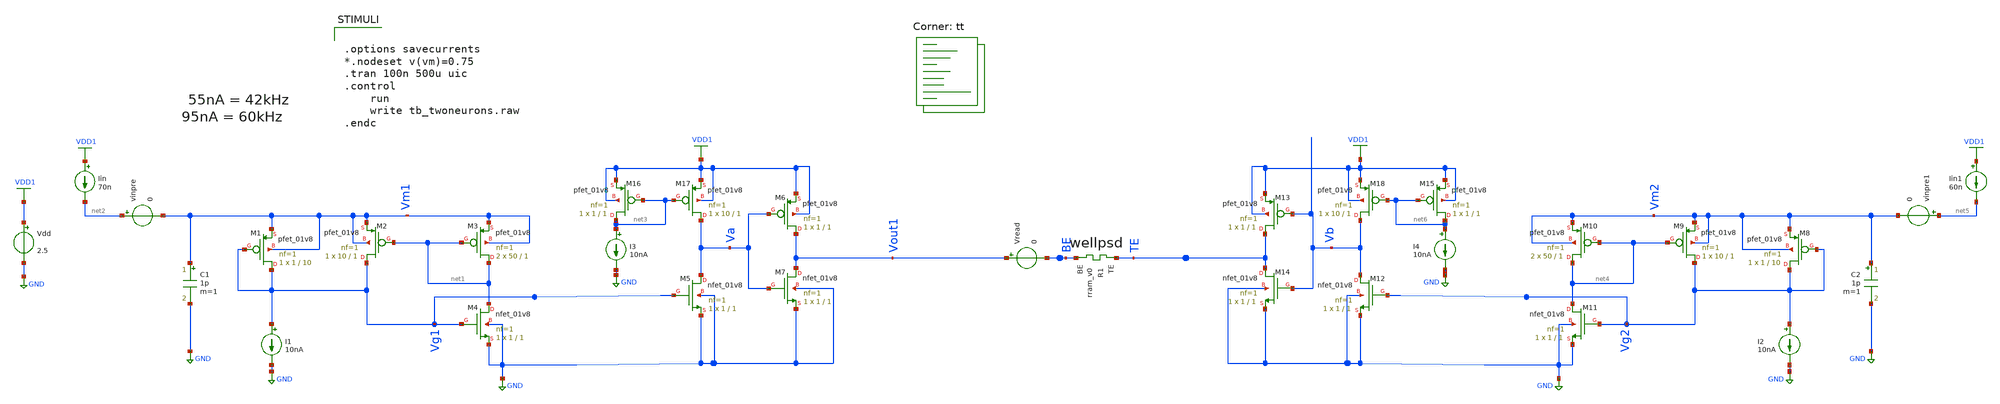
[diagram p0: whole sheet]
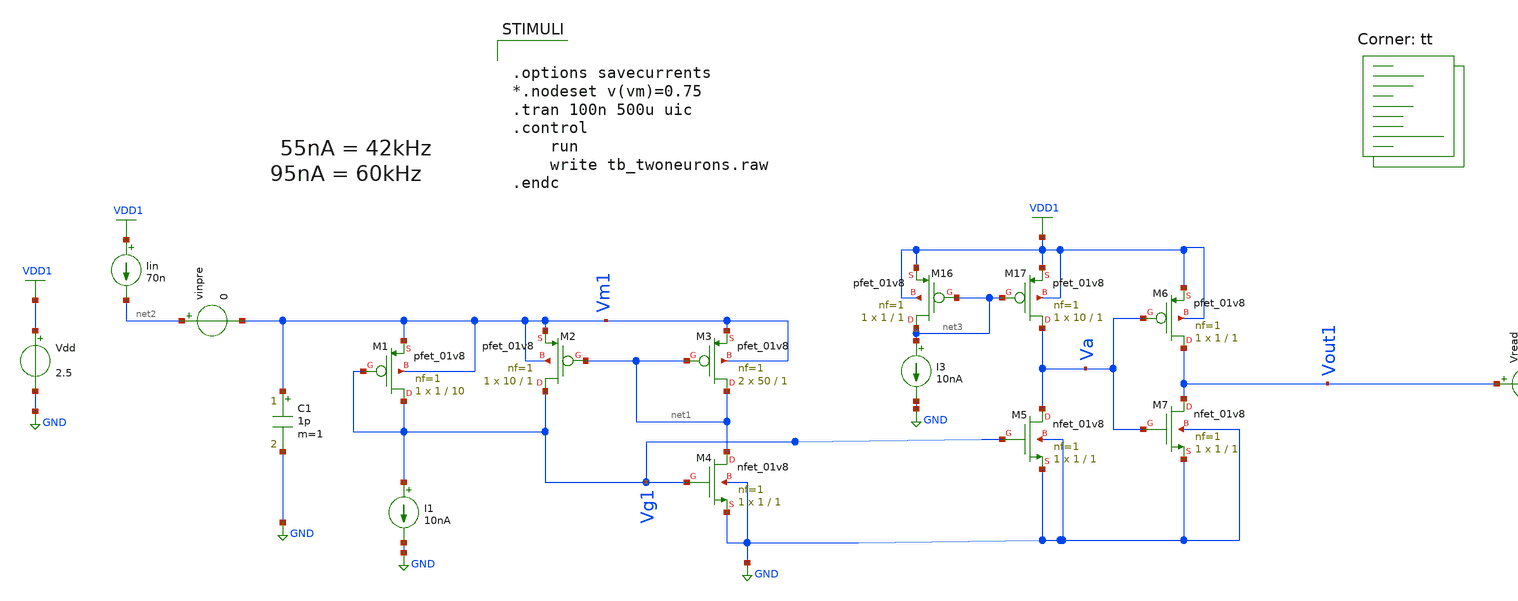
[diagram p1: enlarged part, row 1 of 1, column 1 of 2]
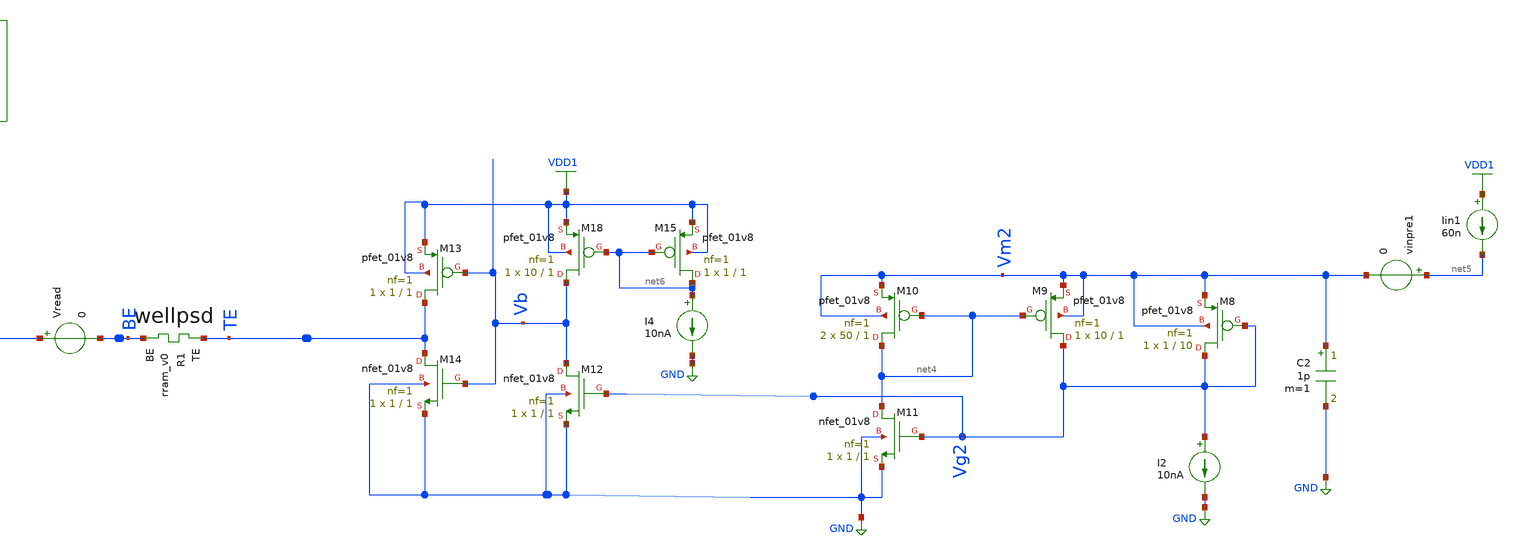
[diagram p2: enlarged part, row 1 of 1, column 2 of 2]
** sch_path: Neuron/ultralif/tb_twoneurons.sch
**.subckt tb_twoneurons
XM1 Vg1 Vg1 Vm1 Vm1 sky130_fd_pr__pfet_01v8 L=10 W=1 nf=1 ad='int((nf+1)/2) * W/nf * 0.29' as='int((nf+2)/2) * W/nf * 0.29'
+ pd='2*int((nf+1)/2) * (W/nf + 0.29)' ps='2*int((nf+2)/2) * (W/nf + 0.29)' nrd='0.29 / W' nrs='0.29 / W'
+ sa=0 sb=0 sd=0 mult=1 m=1
XM2 Vg1 net1 Vm1 Vm1 sky130_fd_pr__pfet_01v8 L=1 W=10 nf=1 ad='int((nf+1)/2) * W/nf * 0.29' as='int((nf+2)/2) * W/nf * 0.29'
+ pd='2*int((nf+1)/2) * (W/nf + 0.29)' ps='2*int((nf+2)/2) * (W/nf + 0.29)' nrd='0.29 / W' nrs='0.29 / W'
+ sa=0 sb=0 sd=0 mult=1 m=1
XM3 net1 net1 Vm1 Vm1 sky130_fd_pr__pfet_01v8 L=1 W=50 nf=1 ad='int((nf+1)/2) * W/nf * 0.29' as='int((nf+2)/2) * W/nf * 0.29'
+ pd='2*int((nf+1)/2) * (W/nf + 0.29)' ps='2*int((nf+2)/2) * (W/nf + 0.29)' nrd='0.29 / W' nrs='0.29 / W'
+ sa=0 sb=0 sd=0 mult=2 m=2
XM4 net1 Vg1 GND GND sky130_fd_pr__nfet_01v8 L=1 W=1 nf=1 ad='int((1 + 1)/2) * 1 / 1 * 0.29' as='int((1 + 2)/2) * 1 / 1 * 0.29'
+ pd='2*int((1 + 1)/2) * (1 / 1 + 0.29)' ps='2*int((1 + 2)/2) * (1 / 1 + 0.29)' nrd='0.29 / 1 ' nrs='0.29 / 1 '
+ sa=0 sb=0 sd=0 mult=1 m=1
XM5 Va Vg1 GND GND sky130_fd_pr__nfet_01v8 L=1 W=1 nf=1 ad='int((1 + 1)/2) * 1 / 1 * 0.29' as='int((1 + 2)/2) * 1 / 1 * 0.29'
+ pd='2*int((1 + 1)/2) * (1 / 1 + 0.29)' ps='2*int((1 + 2)/2) * (1 / 1 + 0.29)' nrd='0.29 / 1 ' nrs='0.29 / 1 '
+ sa=0 sb=0 sd=0 mult=1 m=1
XM6 Vout1 Va VDD1 VDD1 sky130_fd_pr__pfet_01v8 L=1 W=1 nf=1 ad='int((nf+1)/2) * W/nf * 0.29' as='int((nf+2)/2) * W/nf * 0.29'
+ pd='2*int((nf+1)/2) * (W/nf + 0.29)' ps='2*int((nf+2)/2) * (W/nf + 0.29)' nrd='0.29 / W' nrs='0.29 / W'
+ sa=0 sb=0 sd=0 mult=1 m=1
XM7 Vout1 Va GND GND sky130_fd_pr__nfet_01v8 L=1 W=1 nf=1 ad='int((1 + 1)/2) * 1 / 1 * 0.29' as='int((1 + 2)/2) * 1 / 1 * 0.29'
+ pd='2*int((1 + 1)/2) * (1 / 1 + 0.29)' ps='2*int((1 + 2)/2) * (1 / 1 + 0.29)' nrd='0.29 / 1 ' nrs='0.29 / 1 '
+ sa=0 sb=0 sd=0 mult=1 m=1
I1 Vg1 GND 10nA
C1 Vm1 GND 1p m=1
Iin VDD1 net2 70n
I3 net3 GND 10nA
Vdd VDD1 GND 2.5
XR1 TE BE rram_v0
vinpre net2 Vm1 0
XM16 net3 net3 VDD1 VDD1 sky130_fd_pr__pfet_01v8 L=1 W=1 nf=1 ad='int((nf+1)/2) * W/nf * 0.29' as='int((nf+2)/2) * W/nf * 0.29'
+ pd='2*int((nf+1)/2) * (W/nf + 0.29)' ps='2*int((nf+2)/2) * (W/nf + 0.29)' nrd='0.29 / W' nrs='0.29 / W'
+ sa=0 sb=0 sd=0 mult=1 m=1
XM17 Va net3 VDD1 VDD1 sky130_fd_pr__pfet_01v8 L=1 W=10 nf=1 ad='int((nf+1)/2) * W/nf * 0.29' as='int((nf+2)/2) * W/nf * 0.29'
+ pd='2*int((nf+1)/2) * (W/nf + 0.29)' ps='2*int((nf+2)/2) * (W/nf + 0.29)' nrd='0.29 / W' nrs='0.29 / W'
+ sa=0 sb=0 sd=0 mult=1 m=1
XM8 Vg2 Vg2 Vm2 Vm2 sky130_fd_pr__pfet_01v8 L=10 W=1 nf=1 ad='int((nf+1)/2) * W/nf * 0.29' as='int((nf+2)/2) * W/nf * 0.29'
+ pd='2*int((nf+1)/2) * (W/nf + 0.29)' ps='2*int((nf+2)/2) * (W/nf + 0.29)' nrd='0.29 / W' nrs='0.29 / W'
+ sa=0 sb=0 sd=0 mult=1 m=1
XM9 Vg2 net4 Vm2 Vm2 sky130_fd_pr__pfet_01v8 L=1 W=10 nf=1 ad='int((nf+1)/2) * W/nf * 0.29' as='int((nf+2)/2) * W/nf * 0.29'
+ pd='2*int((nf+1)/2) * (W/nf + 0.29)' ps='2*int((nf+2)/2) * (W/nf + 0.29)' nrd='0.29 / W' nrs='0.29 / W'
+ sa=0 sb=0 sd=0 mult=1 m=1
XM10 net4 net4 Vm2 Vm2 sky130_fd_pr__pfet_01v8 L=1 W=50 nf=1 ad='int((nf+1)/2) * W/nf * 0.29' as='int((nf+2)/2) * W/nf * 0.29'
+ pd='2*int((nf+1)/2) * (W/nf + 0.29)' ps='2*int((nf+2)/2) * (W/nf + 0.29)' nrd='0.29 / W' nrs='0.29 / W'
+ sa=0 sb=0 sd=0 mult=2 m=2
XM11 net4 Vg2 GND GND sky130_fd_pr__nfet_01v8 L=1 W=1 nf=1 ad='int((1 + 1)/2) * 1 / 1 * 0.29' as='int((1 + 2)/2) * 1 / 1 * 0.29'
+ pd='2*int((1 + 1)/2) * (1 / 1 + 0.29)' ps='2*int((1 + 2)/2) * (1 / 1 + 0.29)' nrd='0.29 / 1 ' nrs='0.29 / 1 '
+ sa=0 sb=0 sd=0 mult=1 m=1
XM12 Vb Vg2 GND GND sky130_fd_pr__nfet_01v8 L=1 W=1 nf=1 ad='int((1 + 1)/2) * 1 / 1 * 0.29' as='int((1 + 2)/2) * 1 / 1 * 0.29'
+ pd='2*int((1 + 1)/2) * (1 / 1 + 0.29)' ps='2*int((1 + 2)/2) * (1 / 1 + 0.29)' nrd='0.29 / 1 ' nrs='0.29 / 1 '
+ sa=0 sb=0 sd=0 mult=1 m=1
XM13 TE Vb VDD1 VDD1 sky130_fd_pr__pfet_01v8 L=1 W=1 nf=1 ad='int((nf+1)/2) * W/nf * 0.29' as='int((nf+2)/2) * W/nf * 0.29'
+ pd='2*int((nf+1)/2) * (W/nf + 0.29)' ps='2*int((nf+2)/2) * (W/nf + 0.29)' nrd='0.29 / W' nrs='0.29 / W'
+ sa=0 sb=0 sd=0 mult=1 m=1
XM14 TE Vb GND GND sky130_fd_pr__nfet_01v8 L=1 W=1 nf=1 ad='int((1 + 1)/2) * 1 / 1 * 0.29' as='int((1 + 2)/2) * 1 / 1 * 0.29'
+ pd='2*int((1 + 1)/2) * (1 / 1 + 0.29)' ps='2*int((1 + 2)/2) * (1 / 1 + 0.29)' nrd='0.29 / 1 ' nrs='0.29 / 1 '
+ sa=0 sb=0 sd=0 mult=1 m=1
I2 Vg2 GND 10nA
C2 Vm2 GND 1p m=1
Iin1 VDD1 net5 60n
I4 net6 GND 10nA
vinpre1 net5 Vm2 0
XM15 net6 net6 VDD1 VDD1 sky130_fd_pr__pfet_01v8 L=1 W=1 nf=1 ad='int((nf+1)/2) * W/nf * 0.29' as='int((nf+2)/2) * W/nf * 0.29'
+ pd='2*int((nf+1)/2) * (W/nf + 0.29)' ps='2*int((nf+2)/2) * (W/nf + 0.29)' nrd='0.29 / W' nrs='0.29 / W'
+ sa=0 sb=0 sd=0 mult=1 m=1
XM18 Vb net6 VDD1 VDD1 sky130_fd_pr__pfet_01v8 L=1 W=10 nf=1 ad='int((nf+1)/2) * W/nf * 0.29' as='int((nf+2)/2) * W/nf * 0.29'
+ pd='2*int((nf+1)/2) * (W/nf + 0.29)' ps='2*int((nf+2)/2) * (W/nf + 0.29)' nrd='0.29 / W' nrs='0.29 / W'
+ sa=0 sb=0 sd=0 mult=1 m=1
Vread Vout1 BE 0
**** begin user architecture code
.lib $::SKYWATER_MODELS/sky130.lib.spice tt

** opencircuitdesign pdks install
.inc $::SKYWATER_MODELS/rram_v0.spice

**** end user architecture code
**.ends
.GLOBAL GND
.GLOBAL VDD1
**** begin user architecture code


.options savecurrents
*.nodeset v(vm)=0.75
.tran 100n 500u uic
.control
	run
	write tb_twoneurons.raw
.endc


**** end user architecture code
.end
